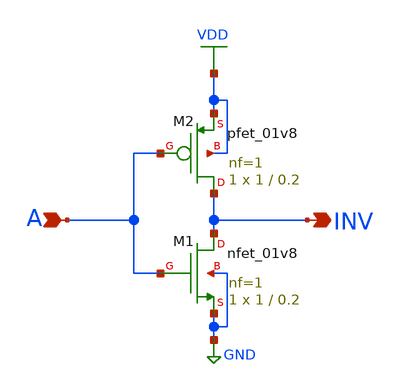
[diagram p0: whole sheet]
** sch_path: skywater_stuff/INV.sch
**.subckt INV INV A
*.opin INV
*.ipin A
XM1 INV A GND GND sky130_fd_pr__nfet_01v8 L=0.2 W=1 nf=1 ad='int((nf+1)/2) * W/nf * 0.29' as='int((nf+2)/2) * W/nf * 0.29'
+ pd='2*int((nf+1)/2) * (W/nf + 0.29)' ps='2*int((nf+2)/2) * (W/nf + 0.29)' nrd='0.29 / W' nrs='0.29 / W'
+ sa=0 sb=0 sd=0 mult=1 m=1
XM2 INV A VDD VDD sky130_fd_pr__pfet_01v8 L=0.2 W=1 nf=1 ad='int((nf+1)/2) * W/nf * 0.29' as='int((nf+2)/2) * W/nf * 0.29'
+ pd='2*int((nf+1)/2) * (W/nf + 0.29)' ps='2*int((nf+2)/2) * (W/nf + 0.29)' nrd='0.29 / W' nrs='0.29 / W'
+ sa=0 sb=0 sd=0 mult=1 m=1
**.ends
.GLOBAL GND
.GLOBAL VDD
.end
